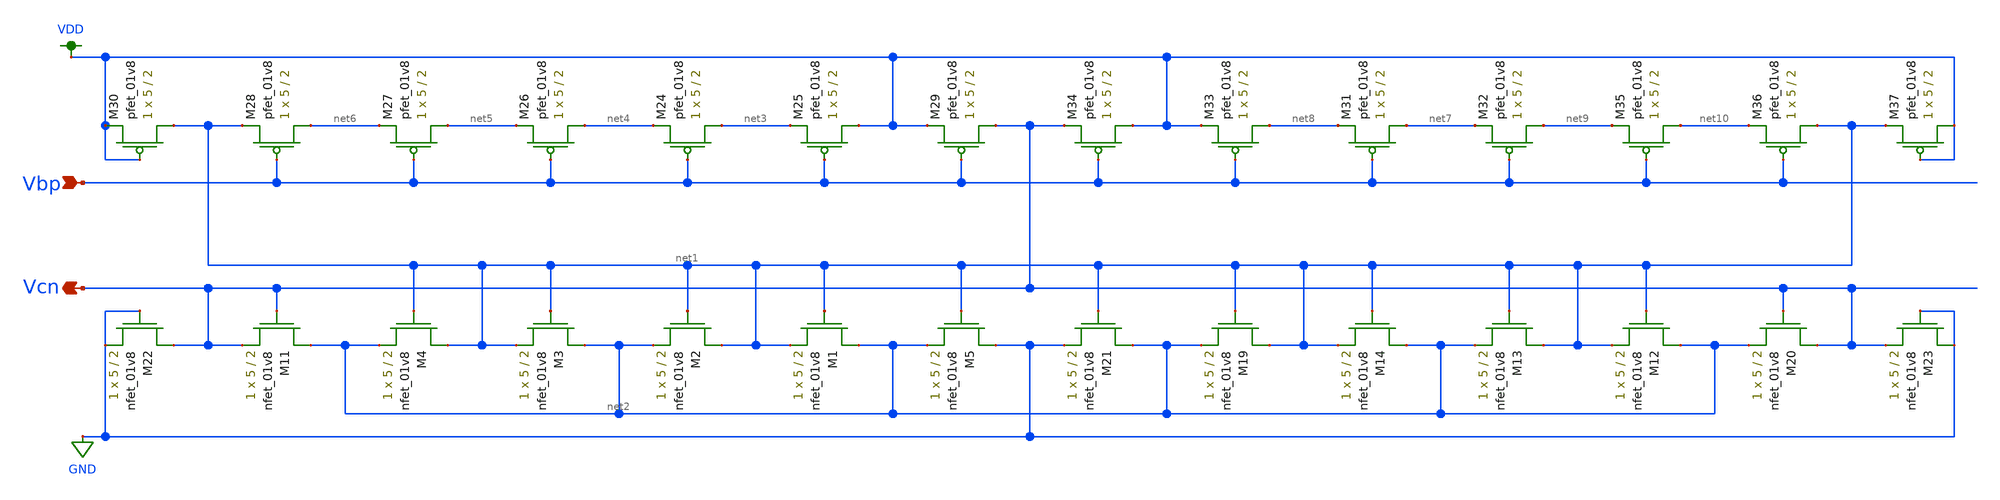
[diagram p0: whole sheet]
** sch_path: schematic/cascode_generator_LDS.sch
**.subckt cascode_generator_LDS Vcn Vbp
*.opin Vcn
*.ipin Vbp
XM1 net2 net1 net1 GND sky130_fd_pr__nfet_01v8 L=2 W=5 nf=1 ad='int((nf+1)/2) * W/nf * 0.29' as='int((nf+2)/2) * W/nf * 0.29'
+ pd='2*int((nf+1)/2) * (W/nf + 0.29)' ps='2*int((nf+2)/2) * (W/nf + 0.29)' nrd='0.29 / W' nrs='0.29 / W'
+ sa=0 sb=0 sd=0 mult=1 m=1
XM2 net1 net1 net2 GND sky130_fd_pr__nfet_01v8 L=2 W=5 nf=1 ad='int((nf+1)/2) * W/nf * 0.29' as='int((nf+2)/2) * W/nf * 0.29'
+ pd='2*int((nf+1)/2) * (W/nf + 0.29)' ps='2*int((nf+2)/2) * (W/nf + 0.29)' nrd='0.29 / W' nrs='0.29 / W'
+ sa=0 sb=0 sd=0 mult=1 m=1
XM3 net2 net1 net1 GND sky130_fd_pr__nfet_01v8 L=2 W=5 nf=1 ad='int((nf+1)/2) * W/nf * 0.29' as='int((nf+2)/2) * W/nf * 0.29'
+ pd='2*int((nf+1)/2) * (W/nf + 0.29)' ps='2*int((nf+2)/2) * (W/nf + 0.29)' nrd='0.29 / W' nrs='0.29 / W'
+ sa=0 sb=0 sd=0 mult=1 m=1
XM4 net1 net1 net2 GND sky130_fd_pr__nfet_01v8 L=2 W=5 nf=1 ad='int((nf+1)/2) * W/nf * 0.29' as='int((nf+2)/2) * W/nf * 0.29'
+ pd='2*int((nf+1)/2) * (W/nf + 0.29)' ps='2*int((nf+2)/2) * (W/nf + 0.29)' nrd='0.29 / W' nrs='0.29 / W'
+ sa=0 sb=0 sd=0 mult=1 m=1
XM5 GND net1 net2 GND sky130_fd_pr__nfet_01v8 L=2 W=5 nf=1 ad='int((nf+1)/2) * W/nf * 0.29' as='int((nf+2)/2) * W/nf * 0.29'
+ pd='2*int((nf+1)/2) * (W/nf + 0.29)' ps='2*int((nf+2)/2) * (W/nf + 0.29)' nrd='0.29 / W' nrs='0.29 / W'
+ sa=0 sb=0 sd=0 mult=1 m=1
XM11 net2 Vcn Vcn GND sky130_fd_pr__nfet_01v8 L=2 W=5 nf=1 ad='int((nf+1)/2) * W/nf * 0.29' as='int((nf+2)/2) * W/nf * 0.29'
+ pd='2*int((nf+1)/2) * (W/nf + 0.29)' ps='2*int((nf+2)/2) * (W/nf + 0.29)' nrd='0.29 / W' nrs='0.29 / W'
+ sa=0 sb=0 sd=0 mult=1 m=1
XM12 net2 net1 net1 GND sky130_fd_pr__nfet_01v8 L=2 W=5 nf=1 ad='int((nf+1)/2) * W/nf * 0.29' as='int((nf+2)/2) * W/nf * 0.29'
+ pd='2*int((nf+1)/2) * (W/nf + 0.29)' ps='2*int((nf+2)/2) * (W/nf + 0.29)' nrd='0.29 / W' nrs='0.29 / W'
+ sa=0 sb=0 sd=0 mult=1 m=1
XM13 net1 net1 net2 GND sky130_fd_pr__nfet_01v8 L=2 W=5 nf=1 ad='int((nf+1)/2) * W/nf * 0.29' as='int((nf+2)/2) * W/nf * 0.29'
+ pd='2*int((nf+1)/2) * (W/nf + 0.29)' ps='2*int((nf+2)/2) * (W/nf + 0.29)' nrd='0.29 / W' nrs='0.29 / W'
+ sa=0 sb=0 sd=0 mult=1 m=1
XM14 net2 net1 net1 GND sky130_fd_pr__nfet_01v8 L=2 W=5 nf=1 ad='int((nf+1)/2) * W/nf * 0.29' as='int((nf+2)/2) * W/nf * 0.29'
+ pd='2*int((nf+1)/2) * (W/nf + 0.29)' ps='2*int((nf+2)/2) * (W/nf + 0.29)' nrd='0.29 / W' nrs='0.29 / W'
+ sa=0 sb=0 sd=0 mult=1 m=1
XM19 net1 net1 net2 GND sky130_fd_pr__nfet_01v8 L=2 W=5 nf=1 ad='int((nf+1)/2) * W/nf * 0.29' as='int((nf+2)/2) * W/nf * 0.29'
+ pd='2*int((nf+1)/2) * (W/nf + 0.29)' ps='2*int((nf+2)/2) * (W/nf + 0.29)' nrd='0.29 / W' nrs='0.29 / W'
+ sa=0 sb=0 sd=0 mult=1 m=1
XM20 Vcn Vcn net2 GND sky130_fd_pr__nfet_01v8 L=2 W=5 nf=1 ad='int((nf+1)/2) * W/nf * 0.29' as='int((nf+2)/2) * W/nf * 0.29'
+ pd='2*int((nf+1)/2) * (W/nf + 0.29)' ps='2*int((nf+2)/2) * (W/nf + 0.29)' nrd='0.29 / W' nrs='0.29 / W'
+ sa=0 sb=0 sd=0 mult=1 m=1
XM21 net2 net1 GND GND sky130_fd_pr__nfet_01v8 L=2 W=5 nf=1 ad='int((nf+1)/2) * W/nf * 0.29' as='int((nf+2)/2) * W/nf * 0.29'
+ pd='2*int((nf+1)/2) * (W/nf + 0.29)' ps='2*int((nf+2)/2) * (W/nf + 0.29)' nrd='0.29 / W' nrs='0.29 / W'
+ sa=0 sb=0 sd=0 mult=1 m=1
XM22 Vcn GND GND GND sky130_fd_pr__nfet_01v8 L=2 W=5 nf=1 ad='int((nf+1)/2) * W/nf * 0.29' as='int((nf+2)/2) * W/nf * 0.29'
+ pd='2*int((nf+1)/2) * (W/nf + 0.29)' ps='2*int((nf+2)/2) * (W/nf + 0.29)' nrd='0.29 / W' nrs='0.29 / W'
+ sa=0 sb=0 sd=0 mult=1 m=1
XM23 GND GND Vcn GND sky130_fd_pr__nfet_01v8 L=2 W=5 nf=1 ad='int((nf+1)/2) * W/nf * 0.29' as='int((nf+2)/2) * W/nf * 0.29'
+ pd='2*int((nf+1)/2) * (W/nf + 0.29)' ps='2*int((nf+2)/2) * (W/nf + 0.29)' nrd='0.29 / W' nrs='0.29 / W'
+ sa=0 sb=0 sd=0 mult=1 m=1
XM24 net3 Vbp net4 VDD sky130_fd_pr__pfet_01v8 L=2 W=5 nf=1 ad='int((nf+1)/2) * W/nf * 0.29' as='int((nf+2)/2) * W/nf * 0.29'
+ pd='2*int((nf+1)/2) * (W/nf + 0.29)' ps='2*int((nf+2)/2) * (W/nf + 0.29)' nrd='0.29 / W' nrs='0.29 / W'
+ sa=0 sb=0 sd=0 mult=1 m=1
XM25 VDD Vbp net3 VDD sky130_fd_pr__pfet_01v8 L=2 W=5 nf=1 ad='int((nf+1)/2) * W/nf * 0.29' as='int((nf+2)/2) * W/nf * 0.29'
+ pd='2*int((nf+1)/2) * (W/nf + 0.29)' ps='2*int((nf+2)/2) * (W/nf + 0.29)' nrd='0.29 / W' nrs='0.29 / W'
+ sa=0 sb=0 sd=0 mult=1 m=1
XM26 net4 Vbp net5 VDD sky130_fd_pr__pfet_01v8 L=2 W=5 nf=1 ad='int((nf+1)/2) * W/nf * 0.29' as='int((nf+2)/2) * W/nf * 0.29'
+ pd='2*int((nf+1)/2) * (W/nf + 0.29)' ps='2*int((nf+2)/2) * (W/nf + 0.29)' nrd='0.29 / W' nrs='0.29 / W'
+ sa=0 sb=0 sd=0 mult=1 m=1
XM27 net5 Vbp net6 VDD sky130_fd_pr__pfet_01v8 L=2 W=5 nf=1 ad='int((nf+1)/2) * W/nf * 0.29' as='int((nf+2)/2) * W/nf * 0.29'
+ pd='2*int((nf+1)/2) * (W/nf + 0.29)' ps='2*int((nf+2)/2) * (W/nf + 0.29)' nrd='0.29 / W' nrs='0.29 / W'
+ sa=0 sb=0 sd=0 mult=1 m=1
XM28 net6 Vbp net1 VDD sky130_fd_pr__pfet_01v8 L=2 W=5 nf=1 ad='int((nf+1)/2) * W/nf * 0.29' as='int((nf+2)/2) * W/nf * 0.29'
+ pd='2*int((nf+1)/2) * (W/nf + 0.29)' ps='2*int((nf+2)/2) * (W/nf + 0.29)' nrd='0.29 / W' nrs='0.29 / W'
+ sa=0 sb=0 sd=0 mult=1 m=1
XM29 Vcn Vbp VDD VDD sky130_fd_pr__pfet_01v8 L=2 W=5 nf=1 ad='int((nf+1)/2) * W/nf * 0.29' as='int((nf+2)/2) * W/nf * 0.29'
+ pd='2*int((nf+1)/2) * (W/nf + 0.29)' ps='2*int((nf+2)/2) * (W/nf + 0.29)' nrd='0.29 / W' nrs='0.29 / W'
+ sa=0 sb=0 sd=0 mult=1 m=1
XM30 net1 VDD VDD VDD sky130_fd_pr__pfet_01v8 L=2 W=5 nf=1 ad='int((nf+1)/2) * W/nf * 0.29' as='int((nf+2)/2) * W/nf * 0.29'
+ pd='2*int((nf+1)/2) * (W/nf + 0.29)' ps='2*int((nf+2)/2) * (W/nf + 0.29)' nrd='0.29 / W' nrs='0.29 / W'
+ sa=0 sb=0 sd=0 mult=1 m=1
XM31 net7 Vbp net8 VDD sky130_fd_pr__pfet_01v8 L=2 W=5 nf=1 ad='int((nf+1)/2) * W/nf * 0.29' as='int((nf+2)/2) * W/nf * 0.29'
+ pd='2*int((nf+1)/2) * (W/nf + 0.29)' ps='2*int((nf+2)/2) * (W/nf + 0.29)' nrd='0.29 / W' nrs='0.29 / W'
+ sa=0 sb=0 sd=0 mult=1 m=1
XM32 net9 Vbp net7 VDD sky130_fd_pr__pfet_01v8 L=2 W=5 nf=1 ad='int((nf+1)/2) * W/nf * 0.29' as='int((nf+2)/2) * W/nf * 0.29'
+ pd='2*int((nf+1)/2) * (W/nf + 0.29)' ps='2*int((nf+2)/2) * (W/nf + 0.29)' nrd='0.29 / W' nrs='0.29 / W'
+ sa=0 sb=0 sd=0 mult=1 m=1
XM33 net8 Vbp VDD VDD sky130_fd_pr__pfet_01v8 L=2 W=5 nf=1 ad='int((nf+1)/2) * W/nf * 0.29' as='int((nf+2)/2) * W/nf * 0.29'
+ pd='2*int((nf+1)/2) * (W/nf + 0.29)' ps='2*int((nf+2)/2) * (W/nf + 0.29)' nrd='0.29 / W' nrs='0.29 / W'
+ sa=0 sb=0 sd=0 mult=1 m=1
XM34 VDD Vbp Vcn VDD sky130_fd_pr__pfet_01v8 L=2 W=5 nf=1 ad='int((nf+1)/2) * W/nf * 0.29' as='int((nf+2)/2) * W/nf * 0.29'
+ pd='2*int((nf+1)/2) * (W/nf + 0.29)' ps='2*int((nf+2)/2) * (W/nf + 0.29)' nrd='0.29 / W' nrs='0.29 / W'
+ sa=0 sb=0 sd=0 mult=1 m=1
XM35 net10 Vbp net9 VDD sky130_fd_pr__pfet_01v8 L=2 W=5 nf=1 ad='int((nf+1)/2) * W/nf * 0.29' as='int((nf+2)/2) * W/nf * 0.29'
+ pd='2*int((nf+1)/2) * (W/nf + 0.29)' ps='2*int((nf+2)/2) * (W/nf + 0.29)' nrd='0.29 / W' nrs='0.29 / W'
+ sa=0 sb=0 sd=0 mult=1 m=1
XM36 net1 Vbp net10 VDD sky130_fd_pr__pfet_01v8 L=2 W=5 nf=1 ad='int((nf+1)/2) * W/nf * 0.29' as='int((nf+2)/2) * W/nf * 0.29'
+ pd='2*int((nf+1)/2) * (W/nf + 0.29)' ps='2*int((nf+2)/2) * (W/nf + 0.29)' nrd='0.29 / W' nrs='0.29 / W'
+ sa=0 sb=0 sd=0 mult=1 m=1
XM37 VDD VDD net1 VDD sky130_fd_pr__pfet_01v8 L=2 W=5 nf=1 ad='int((nf+1)/2) * W/nf * 0.29' as='int((nf+2)/2) * W/nf * 0.29'
+ pd='2*int((nf+1)/2) * (W/nf + 0.29)' ps='2*int((nf+2)/2) * (W/nf + 0.29)' nrd='0.29 / W' nrs='0.29 / W'
+ sa=0 sb=0 sd=0 mult=1 m=1
**.ends
.GLOBAL VDD
.GLOBAL GND
.end
